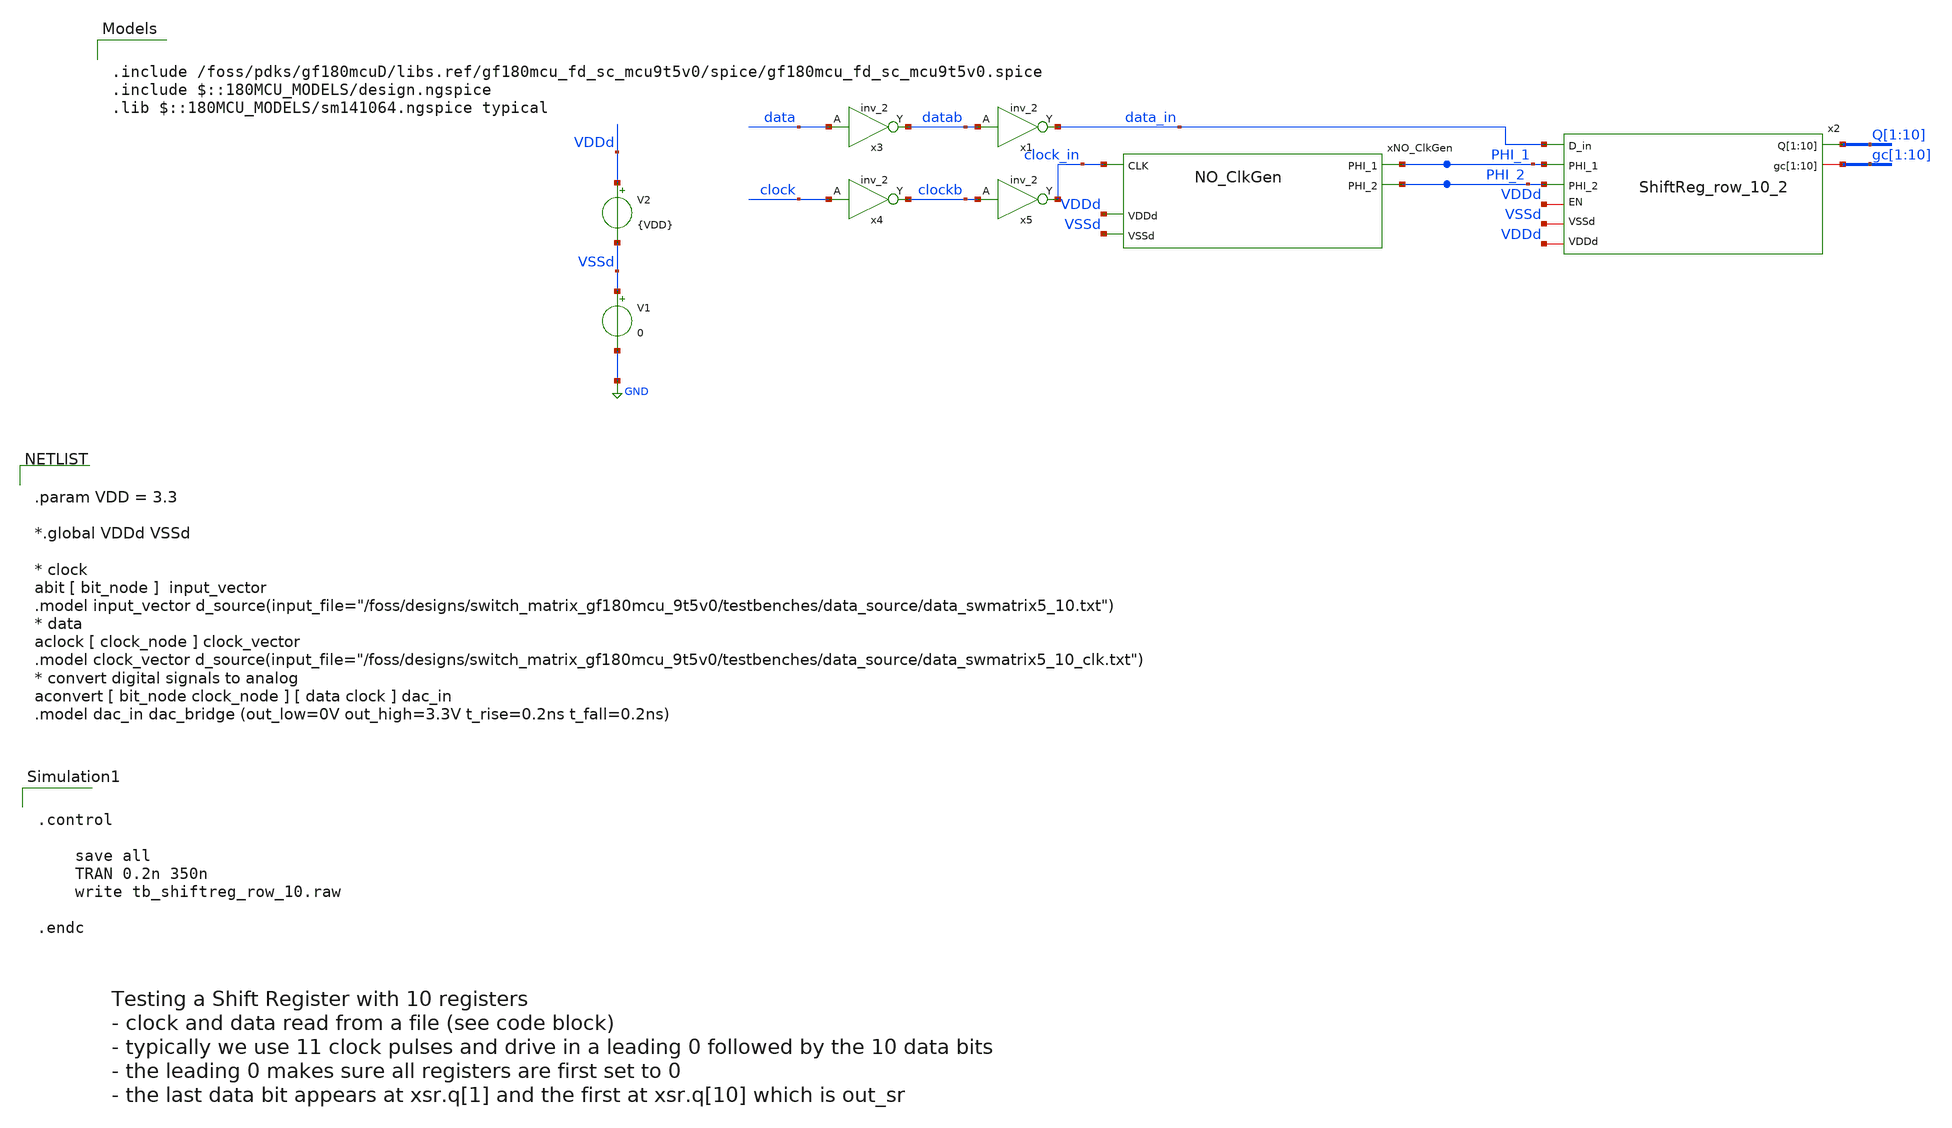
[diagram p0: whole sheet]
** sch_path: testbenches/tb_ShiftReg_row_10.sch
**.subckt tb_ShiftReg_row_10
V1 VSSd GND 0
V2 VDDd VSSd {VDD}
xNO_ClkGen PHI_2 clock_in PHI_1 VDDd VSSd NO_ClkGen
x3 data VSSd VDDd VSSd VDDd datab gf180mcu_fd_sc_mcu9t5v0__inv_2
x1 datab VSSd VDDd VSSd VDDd data_in gf180mcu_fd_sc_mcu9t5v0__inv_2
x4 clock VSSd VDDd VSSd VDDd clockb gf180mcu_fd_sc_mcu9t5v0__inv_2
x5 clockb VSSd VDDd VSSd VDDd clock_in gf180mcu_fd_sc_mcu9t5v0__inv_2
x2 data_in Q[1] Q[2] Q[3] Q[4] Q[5] Q[6] Q[7] Q[8] Q[9] Q[10] gc[1] gc[2] gc[3] gc[4] gc[5] gc[6]
+ gc[7] gc[8] gc[9] gc[10] PHI_1 PHI_2 VDDd VDDd VSSd ShiftReg_row_10_2
**** begin user architecture code

.include /foss/pdks/gf180mcuD/libs.ref/gf180mcu_fd_sc_mcu9t5v0/spice/gf180mcu_fd_sc_mcu9t5v0.spice
.include $::180MCU_MODELS/design.ngspice
.lib $::180MCU_MODELS/sm141064.ngspice typical



.param VDD = 3.3

*.global VDDd VSSd

* clock
abit [ bit_node ]  input_vector
.model input_vector
+ d_source(input_file="/foss/designs/switch_matrix_gf180mcu_9t5v0/testbenches/data_source/data_swmatrix5_10.txt")
* data
aclock [ clock_node ] clock_vector
.model clock_vector
+ d_source(input_file="/foss/designs/switch_matrix_gf180mcu_9t5v0/testbenches/data_source/data_swmatrix5_10_clk.txt")
* convert digital signals to analog
aconvert [ bit_node clock_node ] [ data clock ] dac_in
.model dac_in dac_bridge (out_low=0V out_high=3.3V t_rise=0.2ns t_fall=0.2ns)




.control

    save all
    TRAN 0.2n 350n
    write tb_shiftreg_row_10.raw

.endc


**** end user architecture code
**.ends
.GLOBAL GND
.end
